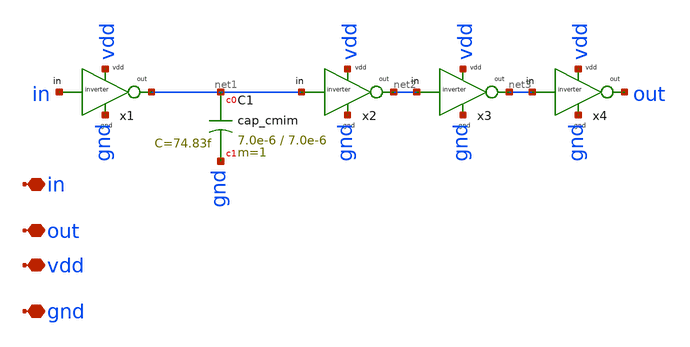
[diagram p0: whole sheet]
** sch_path: dependencies/OTA/OTA-main/schematic/xschem/buffer.sch
**.subckt buffer in out vdd gnd
*.iopin in
*.iopin out
*.iopin vdd
*.iopin gnd
x1 in net1 vdd gnd inverter
x2 net1 net2 vdd gnd inverter
x3 net2 net3 vdd gnd inverter
x4 net3 out vdd gnd inverter
C1 net1 gnd cap_cmim w=7.0e-6 l=7.0e-6 m=1 mm_ok=1
**.ends

* expanding   symbol:
*+  /home/designer/shared/unicass_2026/Design_Files/github_clone_circuit_/UNI-CASS_Project_2025_IIT_DH/Clock_gen_using_transistor_hv/inverter.sym # of pins=4
** sym_path: /home/designer/shared/unicass_2026/Design_Files/github_clone_circuit_/UNI-CASS_Project_2025_IIT_DH/Clock_gen_using_transistor_hv/inverter.sym
** sch_path: /home/designer/shared/unicass_2026/Design_Files/github_clone_circuit_/UNI-CASS_Project_2025_IIT_DH/Clock_gen_using_transistor_hv/inverter.sch
.subckt inverter in out vdd gnd
*.iopin in
*.iopin vdd
*.iopin out
*.iopin gnd
XM3 out in vdd vdd sg13_hv_pmos w=0.6u l=0.9u ng=1 m=1 mm_ok=1
XM1 out in gnd gnd sg13_hv_nmos w=0.3u l=0.45u ng=1 m=1 mm_ok=1
.ends

.end
